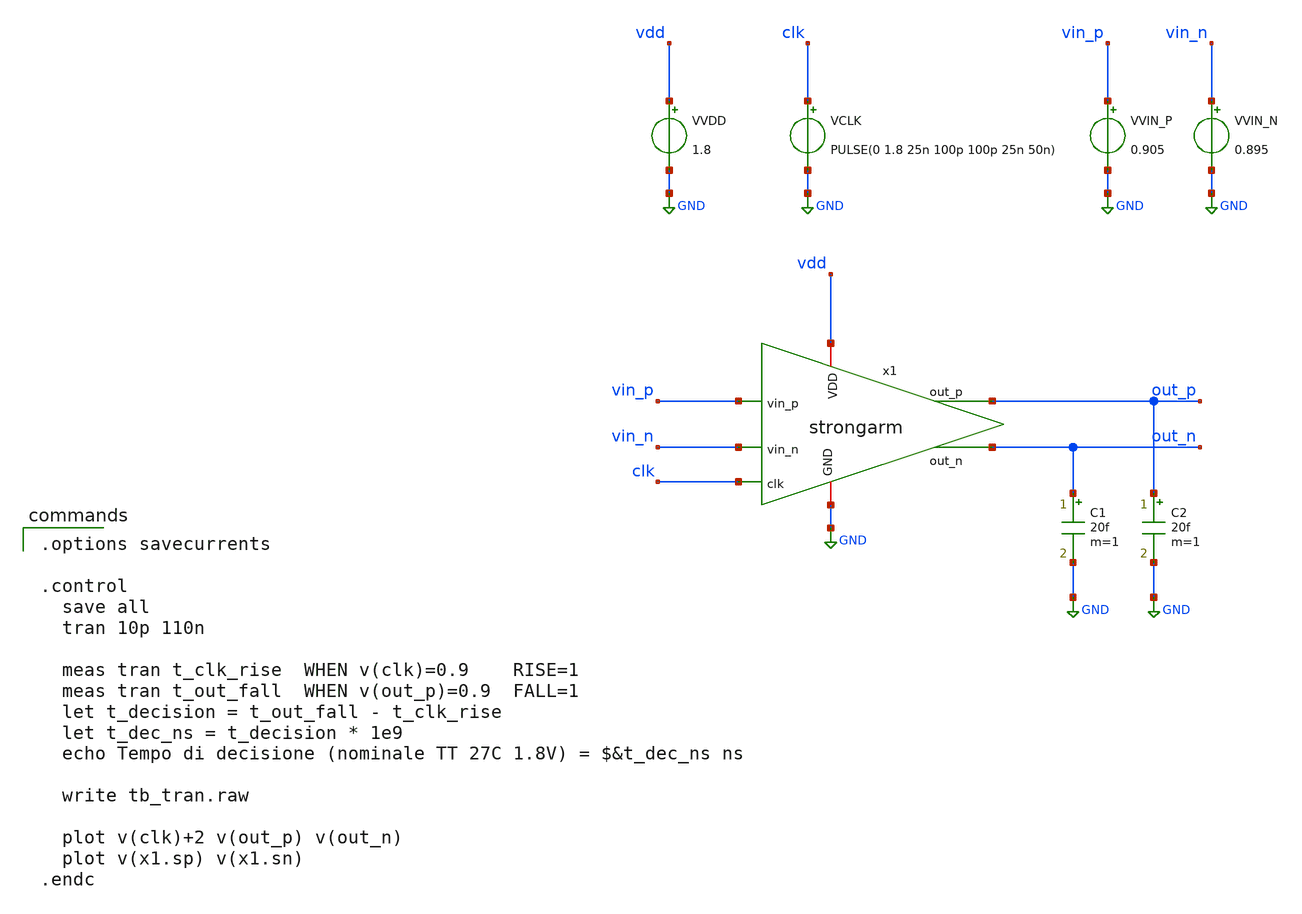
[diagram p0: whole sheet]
** sch_path: 01_xschem_ngspice/soluzioni/lab03/xschem/tb_tran.sch
**.subckt tb_tran
x1 vdd out_p out_n vin_p vin_n clk GND strongarm
VVDD vdd GND 1.8
VCLK clk GND PULSE(0 1.8 25n 100p 100p 25n 50n)
VVIN_P vin_p GND 0.905
VVIN_N vin_n GND 0.895
C1 out_n GND 20f m=1
C2 out_p GND 20f m=1
**** begin user architecture code

** opencircuitdesign pdks install
.lib $::SKYWATER_MODELS/sky130.lib.spice tt


.options savecurrents

.control
  save all
  tran 10p 110n

  meas tran t_clk_rise  WHEN v(clk)=0.9    RISE=1
  meas tran t_out_fall  WHEN v(out_p)=0.9  FALL=1
  let t_decision = t_out_fall - t_clk_rise
  let t_dec_ns = t_decision * 1e9
  echo Tempo di decisione (nominale TT 27C 1.8V) = $&t_dec_ns ns

  write tb_tran.raw

  plot v(clk)+2 v(out_p) v(out_n)
  plot v(x1.sp) v(x1.sn)
.endc

**** end user architecture code
**.ends
.GLOBAL GND
.end
